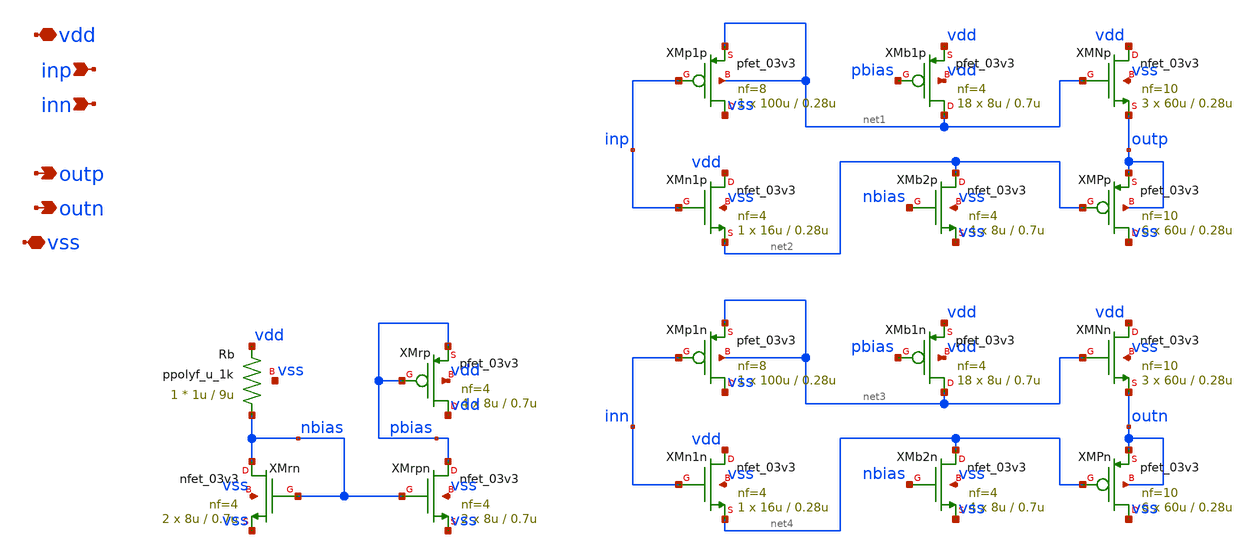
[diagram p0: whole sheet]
** sch_path: blocks/adc/comp-array/buffer.sch
**.subckt buffer vdd inp outp outn vss inn
*.iopin vdd
*.ipin inp
*.opin outp
*.opin outn
*.iopin vss
*.ipin inn
XRb nbias vdd vss ppolyf_u_1k r_width=1u r_length=9u m=1
XMrp vdd pbias pbias vdd pfet_03v3 L=0.7u W=8u nf=4 ad='int((nf+1)/2) * W/nf * 0.18u' as='int((nf+2)/2) * W/nf * 0.18u'
+ pd='2*int((nf+1)/2) * (W/nf + 0.18u)' ps='2*int((nf+2)/2) * (W/nf + 0.18u)' nrd='0.18u / W' nrs='0.18u / W'
+ sa=0 sb=0 sd=0 m=4
XMrn nbias nbias vss vss nfet_03v3 L=0.7u W=8u nf=4 ad='int((nf+1)/2) * W/nf * 0.18u' as='int((nf+2)/2) * W/nf * 0.18u'
+ pd='2*int((nf+1)/2) * (W/nf + 0.18u)' ps='2*int((nf+2)/2) * (W/nf + 0.18u)' nrd='0.18u / W' nrs='0.18u / W'
+ sa=0 sb=0 sd=0 m=2
XMrpn pbias nbias vss vss nfet_03v3 L=0.7u W=8u nf=4 ad='int((nf+1)/2) * W/nf * 0.18u' as='int((nf+2)/2) * W/nf * 0.18u'
+ pd='2*int((nf+1)/2) * (W/nf + 0.18u)' ps='2*int((nf+2)/2) * (W/nf + 0.18u)' nrd='0.18u / W' nrs='0.18u / W'
+ sa=0 sb=0 sd=0 m=2
XMp1p vss inp net1 net1 pfet_03v3 L=0.28u W=100u nf=8 ad='int((nf+1)/2) * W/nf * 0.18u' as='int((nf+2)/2) * W/nf * 0.18u'
+ pd='2*int((nf+1)/2) * (W/nf + 0.18u)' ps='2*int((nf+2)/2) * (W/nf + 0.18u)' nrd='0.18u / W' nrs='0.18u / W'
+ sa=0 sb=0 sd=0 m=1
XMb1p net1 pbias vdd vdd pfet_03v3 L=0.7u W=8u nf=4 ad='int((nf+1)/2) * W/nf * 0.18u' as='int((nf+2)/2) * W/nf * 0.18u'
+ pd='2*int((nf+1)/2) * (W/nf + 0.18u)' ps='2*int((nf+2)/2) * (W/nf + 0.18u)' nrd='0.18u / W' nrs='0.18u / W'
+ sa=0 sb=0 sd=0 m=18
XMn1p vdd inp net2 vss nfet_03v3 L=0.28u W=16u nf=4 ad='int((nf+1)/2) * W/nf * 0.18u' as='int((nf+2)/2) * W/nf * 0.18u'
+ pd='2*int((nf+1)/2) * (W/nf + 0.18u)' ps='2*int((nf+2)/2) * (W/nf + 0.18u)' nrd='0.18u / W' nrs='0.18u / W'
+ sa=0 sb=0 sd=0 m=1
XMb2p net2 nbias vss vss nfet_03v3 L=0.7u W=8u nf=4 ad='int((nf+1)/2) * W/nf * 0.18u' as='int((nf+2)/2) * W/nf * 0.18u'
+ pd='2*int((nf+1)/2) * (W/nf + 0.18u)' ps='2*int((nf+2)/2) * (W/nf + 0.18u)' nrd='0.18u / W' nrs='0.18u / W'
+ sa=0 sb=0 sd=0 m=4
XMNp vdd net1 outp vss nfet_03v3 L=0.28u W=60u nf=10 ad='int((nf+1)/2) * W/nf * 0.18u' as='int((nf+2)/2) * W/nf * 0.18u'
+ pd='2*int((nf+1)/2) * (W/nf + 0.18u)' ps='2*int((nf+2)/2) * (W/nf + 0.18u)' nrd='0.18u / W' nrs='0.18u / W'
+ sa=0 sb=0 sd=0 m=3
XMPp vss net2 outp outp pfet_03v3 L=0.28u W=60u nf=10 ad='int((nf+1)/2) * W/nf * 0.18u' as='int((nf+2)/2) * W/nf * 0.18u'
+ pd='2*int((nf+1)/2) * (W/nf + 0.18u)' ps='2*int((nf+2)/2) * (W/nf + 0.18u)' nrd='0.18u / W' nrs='0.18u / W'
+ sa=0 sb=0 sd=0 m=6
XMp1n vss inn net3 net3 pfet_03v3 L=0.28u W=100u nf=8 ad='int((nf+1)/2) * W/nf * 0.18u' as='int((nf+2)/2) * W/nf * 0.18u'
+ pd='2*int((nf+1)/2) * (W/nf + 0.18u)' ps='2*int((nf+2)/2) * (W/nf + 0.18u)' nrd='0.18u / W' nrs='0.18u / W'
+ sa=0 sb=0 sd=0 m=1
XMb1n net3 pbias vdd vdd pfet_03v3 L=0.7u W=8u nf=4 ad='int((nf+1)/2) * W/nf * 0.18u' as='int((nf+2)/2) * W/nf * 0.18u'
+ pd='2*int((nf+1)/2) * (W/nf + 0.18u)' ps='2*int((nf+2)/2) * (W/nf + 0.18u)' nrd='0.18u / W' nrs='0.18u / W'
+ sa=0 sb=0 sd=0 m=18
XMn1n vdd inn net4 vss nfet_03v3 L=0.28u W=16u nf=4 ad='int((nf+1)/2) * W/nf * 0.18u' as='int((nf+2)/2) * W/nf * 0.18u'
+ pd='2*int((nf+1)/2) * (W/nf + 0.18u)' ps='2*int((nf+2)/2) * (W/nf + 0.18u)' nrd='0.18u / W' nrs='0.18u / W'
+ sa=0 sb=0 sd=0 m=1
XMb2n net4 nbias vss vss nfet_03v3 L=0.7u W=8u nf=4 ad='int((nf+1)/2) * W/nf * 0.18u' as='int((nf+2)/2) * W/nf * 0.18u'
+ pd='2*int((nf+1)/2) * (W/nf + 0.18u)' ps='2*int((nf+2)/2) * (W/nf + 0.18u)' nrd='0.18u / W' nrs='0.18u / W'
+ sa=0 sb=0 sd=0 m=4
XMNn vdd net3 outn vss nfet_03v3 L=0.28u W=60u nf=10 ad='int((nf+1)/2) * W/nf * 0.18u' as='int((nf+2)/2) * W/nf * 0.18u'
+ pd='2*int((nf+1)/2) * (W/nf + 0.18u)' ps='2*int((nf+2)/2) * (W/nf + 0.18u)' nrd='0.18u / W' nrs='0.18u / W'
+ sa=0 sb=0 sd=0 m=3
XMPn vss net4 outn outn pfet_03v3 L=0.28u W=60u nf=10 ad='int((nf+1)/2) * W/nf * 0.18u' as='int((nf+2)/2) * W/nf * 0.18u'
+ pd='2*int((nf+1)/2) * (W/nf + 0.18u)' ps='2*int((nf+2)/2) * (W/nf + 0.18u)' nrd='0.18u / W' nrs='0.18u / W'
+ sa=0 sb=0 sd=0 m=6
**.ends
.end
